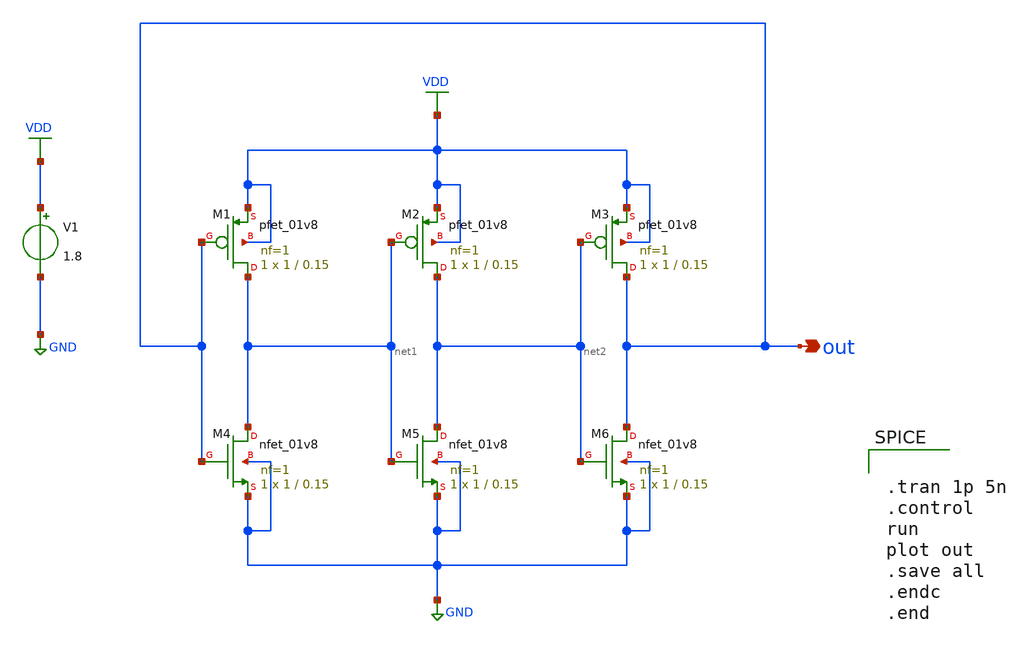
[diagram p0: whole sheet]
** sch_path: Week_3/RingOscillator_PreLayout/RingOscillator_pre.sch
**.subckt RingOscillator_pre out
*.opin out
XM1 net1 out VDD VDD sky130_fd_pr__pfet_01v8 L=0.15 W=1 nf=1 ad='int((nf+1)/2) * W/nf * 0.29' as='int((nf+2)/2) * W/nf * 0.29'
+ pd='2*int((nf+1)/2) * (W/nf + 0.29)' ps='2*int((nf+2)/2) * (W/nf + 0.29)' nrd='0.29 / W' nrs='0.29 / W'
+ sa=0 sb=0 sd=0 mult=1 m=1
XM2 net2 net1 VDD VDD sky130_fd_pr__pfet_01v8 L=0.15 W=1 nf=1 ad='int((nf+1)/2) * W/nf * 0.29' as='int((nf+2)/2) * W/nf * 0.29'
+ pd='2*int((nf+1)/2) * (W/nf + 0.29)' ps='2*int((nf+2)/2) * (W/nf + 0.29)' nrd='0.29 / W' nrs='0.29 / W'
+ sa=0 sb=0 sd=0 mult=1 m=1
XM3 out net2 VDD VDD sky130_fd_pr__pfet_01v8 L=0.15 W=1 nf=1 ad='int((nf+1)/2) * W/nf * 0.29' as='int((nf+2)/2) * W/nf * 0.29'
+ pd='2*int((nf+1)/2) * (W/nf + 0.29)' ps='2*int((nf+2)/2) * (W/nf + 0.29)' nrd='0.29 / W' nrs='0.29 / W'
+ sa=0 sb=0 sd=0 mult=1 m=1
XM4 net1 out GND GND sky130_fd_pr__nfet_01v8 L=0.15 W=1 nf=1 ad='int((nf+1)/2) * W/nf * 0.29' as='int((nf+2)/2) * W/nf * 0.29'
+ pd='2*int((nf+1)/2) * (W/nf + 0.29)' ps='2*int((nf+2)/2) * (W/nf + 0.29)' nrd='0.29 / W' nrs='0.29 / W'
+ sa=0 sb=0 sd=0 mult=1 m=1
XM5 net2 net1 GND GND sky130_fd_pr__nfet_01v8 L=0.15 W=1 nf=1 ad='int((nf+1)/2) * W/nf * 0.29' as='int((nf+2)/2) * W/nf * 0.29'
+ pd='2*int((nf+1)/2) * (W/nf + 0.29)' ps='2*int((nf+2)/2) * (W/nf + 0.29)' nrd='0.29 / W' nrs='0.29 / W'
+ sa=0 sb=0 sd=0 mult=1 m=1
XM6 out net2 GND GND sky130_fd_pr__nfet_01v8 L=0.15 W=1 nf=1 ad='int((nf+1)/2) * W/nf * 0.29' as='int((nf+2)/2) * W/nf * 0.29'
+ pd='2*int((nf+1)/2) * (W/nf + 0.29)' ps='2*int((nf+2)/2) * (W/nf + 0.29)' nrd='0.29 / W' nrs='0.29 / W'
+ sa=0 sb=0 sd=0 mult=1 m=1
V1 VDD GND 1.8
**** begin user architecture code


.lib /home/swagatika/open_pdks/sky130/sky130A/libs.tech/ngspice/sky130.lib.spice tt

.save all





.tran 1p 5n
.control
run
plot out
.save all
.endc
.end


**** end user architecture code
**.ends
.GLOBAL VDD
.GLOBAL GND
.end
